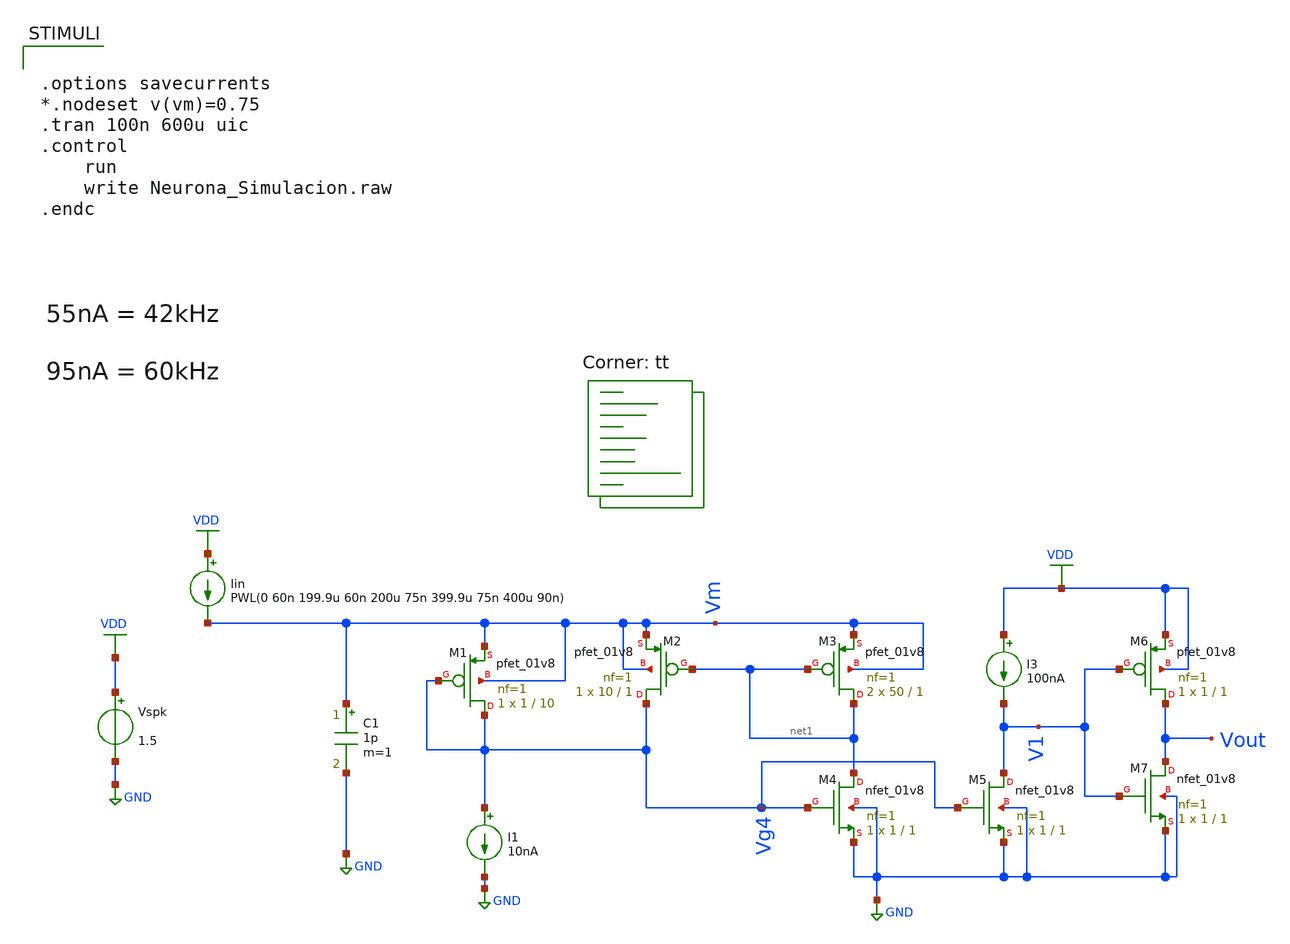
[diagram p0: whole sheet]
** sch_path: Neuron/ultralif/Neurona_Simulacion.sch
**.subckt Neurona_Simulacion
XM1 Vg4 Vg4 Vm Vm sky130_fd_pr__pfet_01v8 L=10 W=1 nf=1 ad='int((nf+1)/2) * W/nf * 0.29' as='int((nf+2)/2) * W/nf * 0.29'
+ pd='2*int((nf+1)/2) * (W/nf + 0.29)' ps='2*int((nf+2)/2) * (W/nf + 0.29)' nrd='0.29 / W' nrs='0.29 / W'
+ sa=0 sb=0 sd=0 mult=1 m=1
XM2 Vg4 net1 Vm Vm sky130_fd_pr__pfet_01v8 L=1 W=10 nf=1 ad='int((nf+1)/2) * W/nf * 0.29' as='int((nf+2)/2) * W/nf * 0.29'
+ pd='2*int((nf+1)/2) * (W/nf + 0.29)' ps='2*int((nf+2)/2) * (W/nf + 0.29)' nrd='0.29 / W' nrs='0.29 / W'
+ sa=0 sb=0 sd=0 mult=1 m=1
XM3 net1 net1 Vm Vm sky130_fd_pr__pfet_01v8 L=1 W=50 nf=1 ad='int((nf+1)/2) * W/nf * 0.29' as='int((nf+2)/2) * W/nf * 0.29'
+ pd='2*int((nf+1)/2) * (W/nf + 0.29)' ps='2*int((nf+2)/2) * (W/nf + 0.29)' nrd='0.29 / W' nrs='0.29 / W'
+ sa=0 sb=0 sd=0 mult=2 m=2
XM4 net1 Vg4 GND GND sky130_fd_pr__nfet_01v8 L=1 W=1 nf=1 ad='int((1 + 1)/2) * 1 / 1 * 0.29' as='int((1 + 2)/2) * 1 / 1 * 0.29'
+ pd='2*int((1 + 1)/2) * (1 / 1 + 0.29)' ps='2*int((1 + 2)/2) * (1 / 1 + 0.29)' nrd='0.29 / 1 ' nrs='0.29 / 1 '
+ sa=0 sb=0 sd=0 mult=1 m=1
XM5 V1 Vg4 GND GND sky130_fd_pr__nfet_01v8 L=1 W=1 nf=1 ad='int((1 + 1)/2) * 1 / 1 * 0.29' as='int((1 + 2)/2) * 1 / 1 * 0.29'
+ pd='2*int((1 + 1)/2) * (1 / 1 + 0.29)' ps='2*int((1 + 2)/2) * (1 / 1 + 0.29)' nrd='0.29 / 1 ' nrs='0.29 / 1 '
+ sa=0 sb=0 sd=0 mult=1 m=1
XM6 Vout V1 VDD VDD sky130_fd_pr__pfet_01v8 L=1 W=1 nf=1 ad='int((nf+1)/2) * W/nf * 0.29' as='int((nf+2)/2) * W/nf * 0.29'
+ pd='2*int((nf+1)/2) * (W/nf + 0.29)' ps='2*int((nf+2)/2) * (W/nf + 0.29)' nrd='0.29 / W' nrs='0.29 / W'
+ sa=0 sb=0 sd=0 mult=1 m=1
XM7 Vout V1 GND GND sky130_fd_pr__nfet_01v8 L=1 W=1 nf=1 ad='int((1 + 1)/2) * 1 / 1 * 0.29' as='int((1 + 2)/2) * 1 / 1 * 0.29'
+ pd='2*int((1 + 1)/2) * (1 / 1 + 0.29)' ps='2*int((1 + 2)/2) * (1 / 1 + 0.29)' nrd='0.29 / 1 ' nrs='0.29 / 1 '
+ sa=0 sb=0 sd=0 mult=1 m=1
I1 Vg4 GND 10nA
Vspk VDD GND 1.5
C1 Vm GND 1p m=1
Iin VDD Vm PWL(0 60n 199.9u 60n 200u 75n 399.9u 75n 400u 90n)
I3 VDD V1 100nA
**** begin user architecture code
.lib $::SKYWATER_MODELS/sky130.lib.spice tt
**** end user architecture code
**.ends
.GLOBAL GND
.GLOBAL VDD
**** begin user architecture code


.options savecurrents
*.nodeset v(vm)=0.75
.tran 100n 600u uic
.control
	run
	write Neurona_Simulacion.raw
.endc


**** end user architecture code
.end
